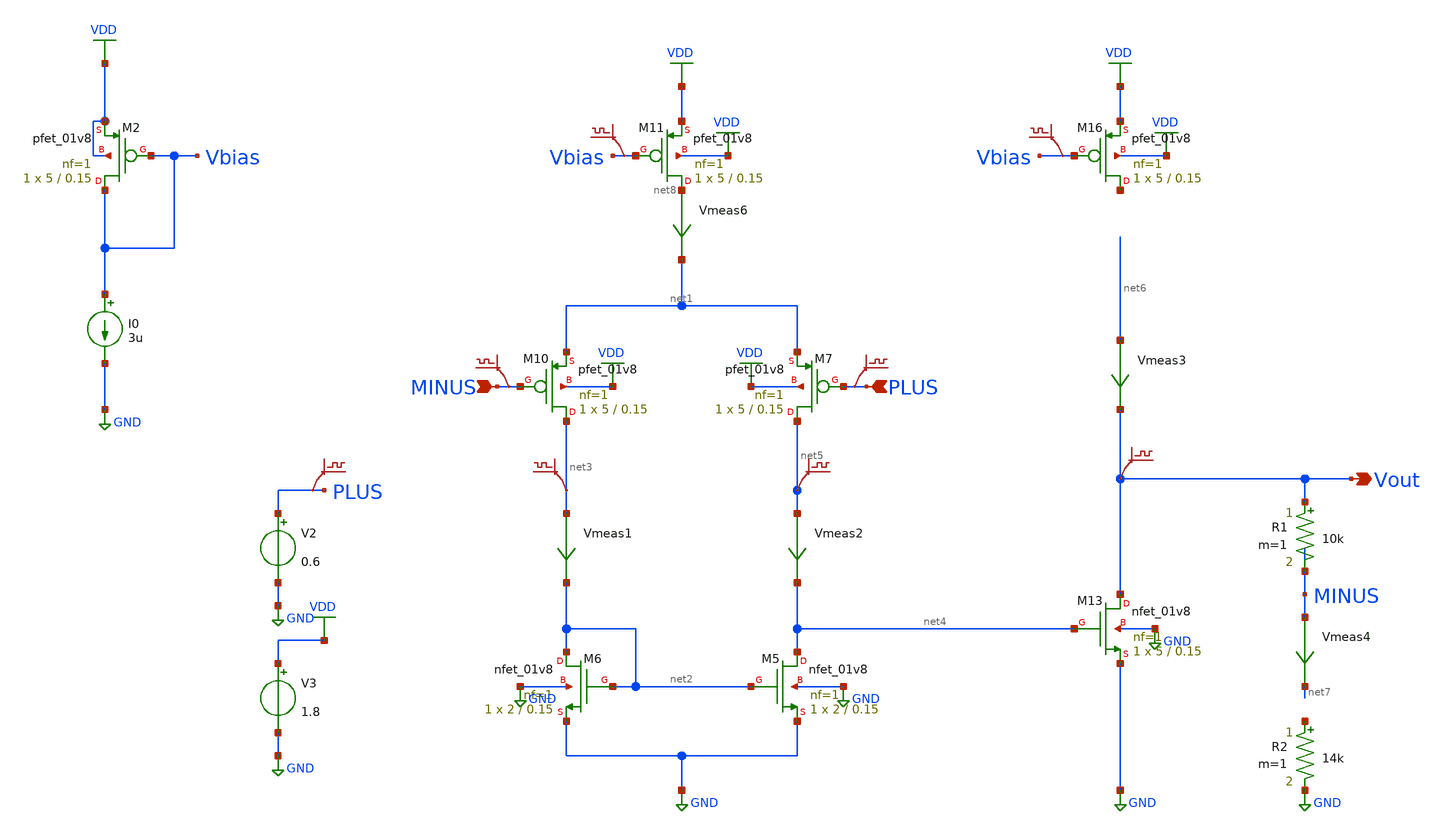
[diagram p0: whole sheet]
** sch_path: lib/xschem/LDO/opamp_2stage.sch
**.subckt opamp_2stage PLUS MINUS Vout
*.ipin PLUS
*.ipin MINUS
*.opin Vout
XM6 net2 net2 GND GND sky130_fd_pr__nfet_01v8 L=0.15 W=2 nf=1 ad='int((nf+1)/2) * W/nf * 0.29' as='int((nf+2)/2) * W/nf * 0.29'
+ pd='2*int((nf+1)/2) * (W/nf + 0.29)' ps='2*int((nf+2)/2) * (W/nf + 0.29)' nrd='0.29 / W' nrs='0.29 / W'
+ sa=0 sb=0 sd=0 mult=1 m=1
XM5 net4 net2 GND GND sky130_fd_pr__nfet_01v8 L=0.15 W=2 nf=1 ad='int((nf+1)/2) * W/nf * 0.29' as='int((nf+2)/2) * W/nf * 0.29'
+ pd='2*int((nf+1)/2) * (W/nf + 0.29)' ps='2*int((nf+2)/2) * (W/nf + 0.29)' nrd='0.29 / W' nrs='0.29 / W'
+ sa=0 sb=0 sd=0 mult=1 m=1
XM7 net5 PLUS net1 VDD sky130_fd_pr__pfet_01v8 L=0.15 W=5 nf=1 ad='int((nf+1)/2) * W/nf * 0.29' as='int((nf+2)/2) * W/nf * 0.29'
+ pd='2*int((nf+1)/2) * (W/nf + 0.29)' ps='2*int((nf+2)/2) * (W/nf + 0.29)' nrd='0.29 / W' nrs='0.29 / W'
+ sa=0 sb=0 sd=0 mult=1 m=1
XM10 net3 MINUS net1 VDD sky130_fd_pr__pfet_01v8 L=0.15 W=5 nf=1 ad='int((nf+1)/2) * W/nf * 0.29' as='int((nf+2)/2) * W/nf * 0.29'
+ pd='2*int((nf+1)/2) * (W/nf + 0.29)' ps='2*int((nf+2)/2) * (W/nf + 0.29)' nrd='0.29 / W' nrs='0.29 / W'
+ sa=0 sb=0 sd=0 mult=1 m=1
XM11 net8 Vbias VDD VDD sky130_fd_pr__pfet_01v8 L=0.15 W=5 nf=1 ad='int((nf+1)/2) * W/nf * 0.29' as='int((nf+2)/2) * W/nf * 0.29'
+ pd='2*int((nf+1)/2) * (W/nf + 0.29)' ps='2*int((nf+2)/2) * (W/nf + 0.29)' nrd='0.29 / W' nrs='0.29 / W'
+ sa=0 sb=0 sd=0 mult=1 m=1
XM13 Vout net4 GND GND sky130_fd_pr__nfet_01v8 L=0.15 W=5 nf=1 ad='int((nf+1)/2) * W/nf * 0.29' as='int((nf+2)/2) * W/nf * 0.29'
+ pd='2*int((nf+1)/2) * (W/nf + 0.29)' ps='2*int((nf+2)/2) * (W/nf + 0.29)' nrd='0.29 / W' nrs='0.29 / W'
+ sa=0 sb=0 sd=0 mult=1 m=1
XM16 net9 Vbias VDD VDD sky130_fd_pr__pfet_01v8 L=0.15 W=5 nf=1 ad='int((nf+1)/2) * W/nf * 0.29' as='int((nf+2)/2) * W/nf * 0.29'
+ pd='2*int((nf+1)/2) * (W/nf + 0.29)' ps='2*int((nf+2)/2) * (W/nf + 0.29)' nrd='0.29 / W' nrs='0.29 / W'
+ sa=0 sb=0 sd=0 mult=1 m=1
V2 PLUS GND 0.6
V3 VDD GND 1.8
.save v(plus)
.save v(minus)
.save v(net5)
.save v(net3)
.save v(vout)
.save v(plus)
Vmeas1 net3 net2 0
.save i(vmeas1)
Vmeas2 net5 net4 0
.save i(vmeas2)
Vmeas3 net6 Vout 0
.save i(vmeas3)
.save v(vbias)
.save v(vbias)
R1 Vout MINUS 10k m=1
R2 net10 GND 14k m=1
Vmeas4 MINUS net7 0
.save i(vmeas4)
Vmeas6 net8 net1 0
.save i(vmeas6)
XM2 Vbias Vbias VDD VDD sky130_fd_pr__pfet_01v8 L=0.15 W=5 nf=1 ad='int((nf+1)/2) * W/nf * 0.29' as='int((nf+2)/2) * W/nf * 0.29'
+ pd='2*int((nf+1)/2) * (W/nf + 0.29)' ps='2*int((nf+2)/2) * (W/nf + 0.29)' nrd='0.29 / W' nrs='0.29 / W'
+ sa=0 sb=0 sd=0 mult=1 m=1
I0 Vbias GND 3u
**** begin user architecture code

.lib $::SKYWATER_MODELS/sky130.lib.spice tt


**** end user architecture code
**.ends
.GLOBAL VDD
.GLOBAL GND
**** begin user architecture code


.save all
.op


**** end user architecture code
.end
